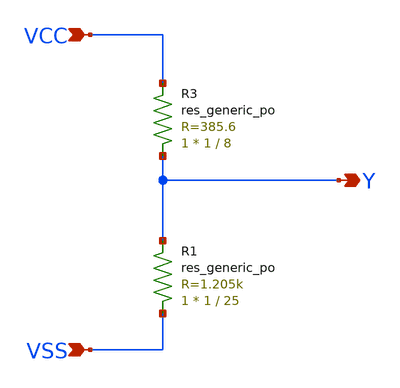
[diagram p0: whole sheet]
** sch_path: xschem/vDivider_25.sch
**.subckt vDivider_25 VCC VSS Y
*.ipin VCC
*.ipin VSS
*.opin Y
XR3 Y VCC sky130_fd_pr__res_generic_po W=1 L=8 m=1
XR1 VSS Y sky130_fd_pr__res_generic_po W=1 L=25 m=1
**.ends
.end
